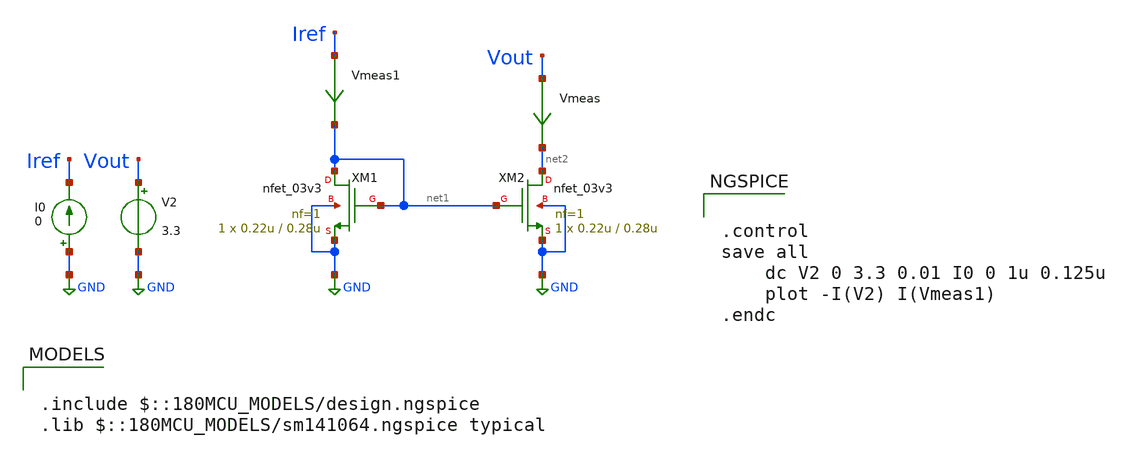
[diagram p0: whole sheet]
** sch_path: week02_current_diffpair/tugas5_cascode_current_mirror/basic-current-mirror.sch
**.subckt basic-current-mirror
XM1 net1 net1 GND GND nfet_03v3 L=0.28u W=0.22u nf=1 ad='int((nf+1)/2) * W/nf * 0.18u' as='int((nf+2)/2) * W/nf * 0.18u'
+ pd='2*int((nf+1)/2) * (W/nf + 0.18u)' ps='2*int((nf+2)/2) * (W/nf + 0.18u)' nrd='0.18u / W' nrs='0.18u / W'
+ sa=0 sb=0 sd=0 m=1
XM2 net2 net1 GND GND nfet_03v3 L=0.28u W=0.22u nf=1 ad='int((nf+1)/2) * W/nf * 0.18u' as='int((nf+2)/2) * W/nf * 0.18u'
+ pd='2*int((nf+1)/2) * (W/nf + 0.18u)' ps='2*int((nf+2)/2) * (W/nf + 0.18u)' nrd='0.18u / W' nrs='0.18u / W'
+ sa=0 sb=0 sd=0 m=1
Vmeas Vout net2 0
.save i(vmeas)
I0 GND Iref 0
V2 Vout GND 3.3
Vmeas1 Iref net1 0
.save i(vmeas1)
**** begin user architecture code

.include $::180MCU_MODELS/design.ngspice
.lib $::180MCU_MODELS/sm141064.ngspice typical



.control
save all
	dc V2 0 3.3 0.01 I0 0 1u 0.125u
	plot -I(V2) I(Vmeas1)
.endc


**** end user architecture code
**.ends
.GLOBAL GND
.end
